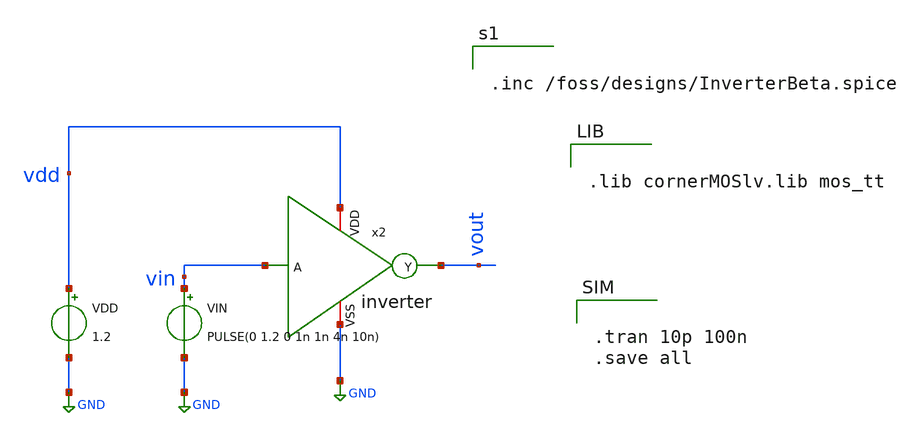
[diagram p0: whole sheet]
** sch_path: InverterBeta_Test.sch
**.subckt InverterBeta_Test
VIN vin GND PULSE(0 1.2 0 1n 1n 4n 10n)
VDD vdd GND 1.2
x2 vdd vin vout GND inverter
**** begin user architecture code


.lib cornerMOSlv.lib mos_tt




.tran 10p 100n
.save all




.inc /foss/designs/InverterBeta.spice


**** end user architecture code
**.ends
.GLOBAL GND
.end
